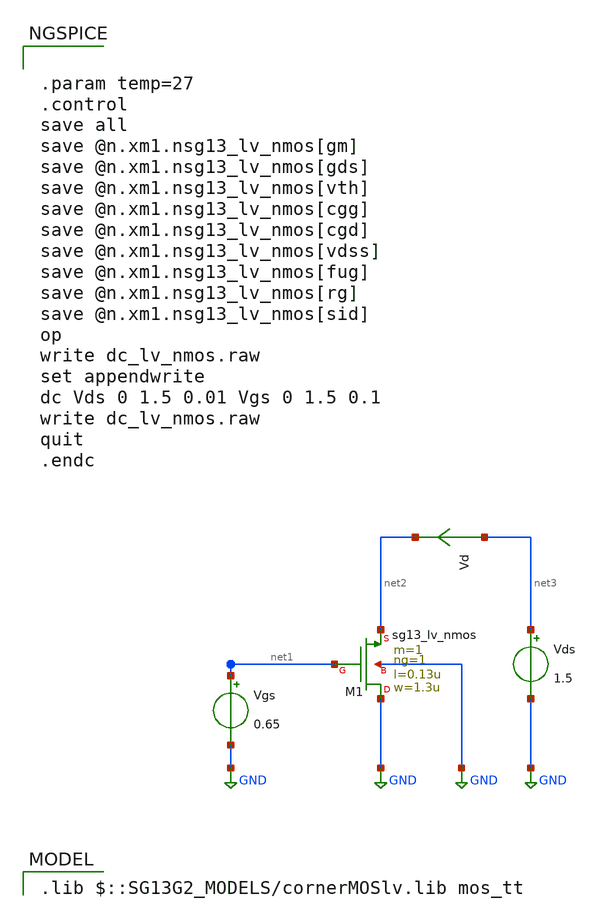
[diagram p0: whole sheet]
** sch_path: xschem/dc_lv_nmos.sch
* Copyright 2023-2024 IHP PDK Authors, Harald Pretl
**.subckt dc_lv_nmos
Vgs net1 GND 0.65
Vds net3 GND 1.5
XM1 GND net1 net2 GND sg13_lv_nmos w=1.3u l=0.13u ng=1 m=1 mm_ok=1
Vd net3 net2 0
.save i(vd)
**** begin user architecture code
 .lib $::SG13G2_MODELS/cornerMOSlv.lib mos_tt



.param temp=27
.control
save all
save @n.xm1.nsg13_lv_nmos[gm]
save @n.xm1.nsg13_lv_nmos[gds]
save @n.xm1.nsg13_lv_nmos[vth]
save @n.xm1.nsg13_lv_nmos[cgg]
save @n.xm1.nsg13_lv_nmos[cgd]
save @n.xm1.nsg13_lv_nmos[vdss]
save @n.xm1.nsg13_lv_nmos[fug]
save @n.xm1.nsg13_lv_nmos[rg]
save @n.xm1.nsg13_lv_nmos[sid]
op
write dc_lv_nmos.raw
set appendwrite
dc Vds 0 1.5 0.01 Vgs 0 1.5 0.1
write dc_lv_nmos.raw
quit
.endc


**** end user architecture code
**.ends
.GLOBAL GND
.end
